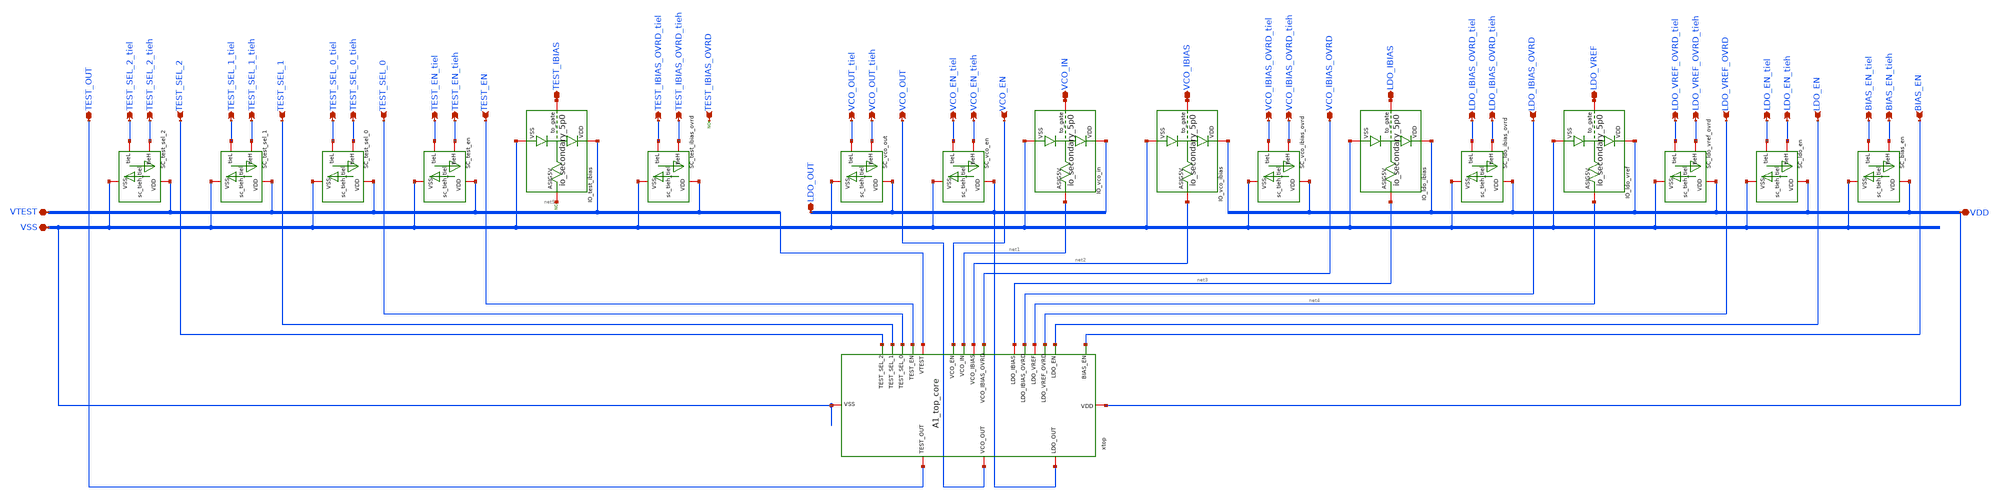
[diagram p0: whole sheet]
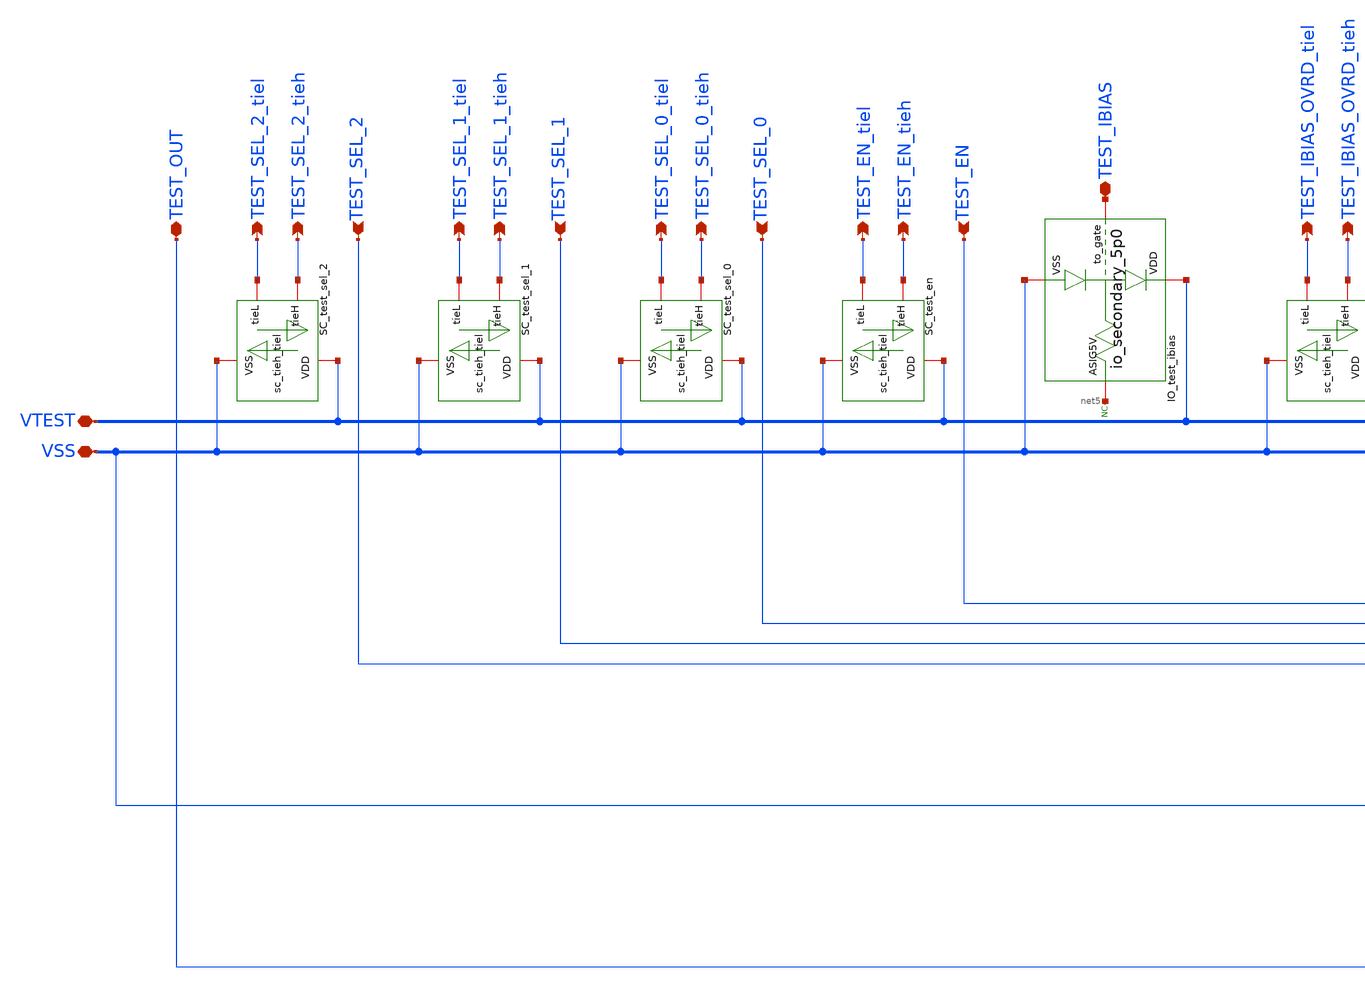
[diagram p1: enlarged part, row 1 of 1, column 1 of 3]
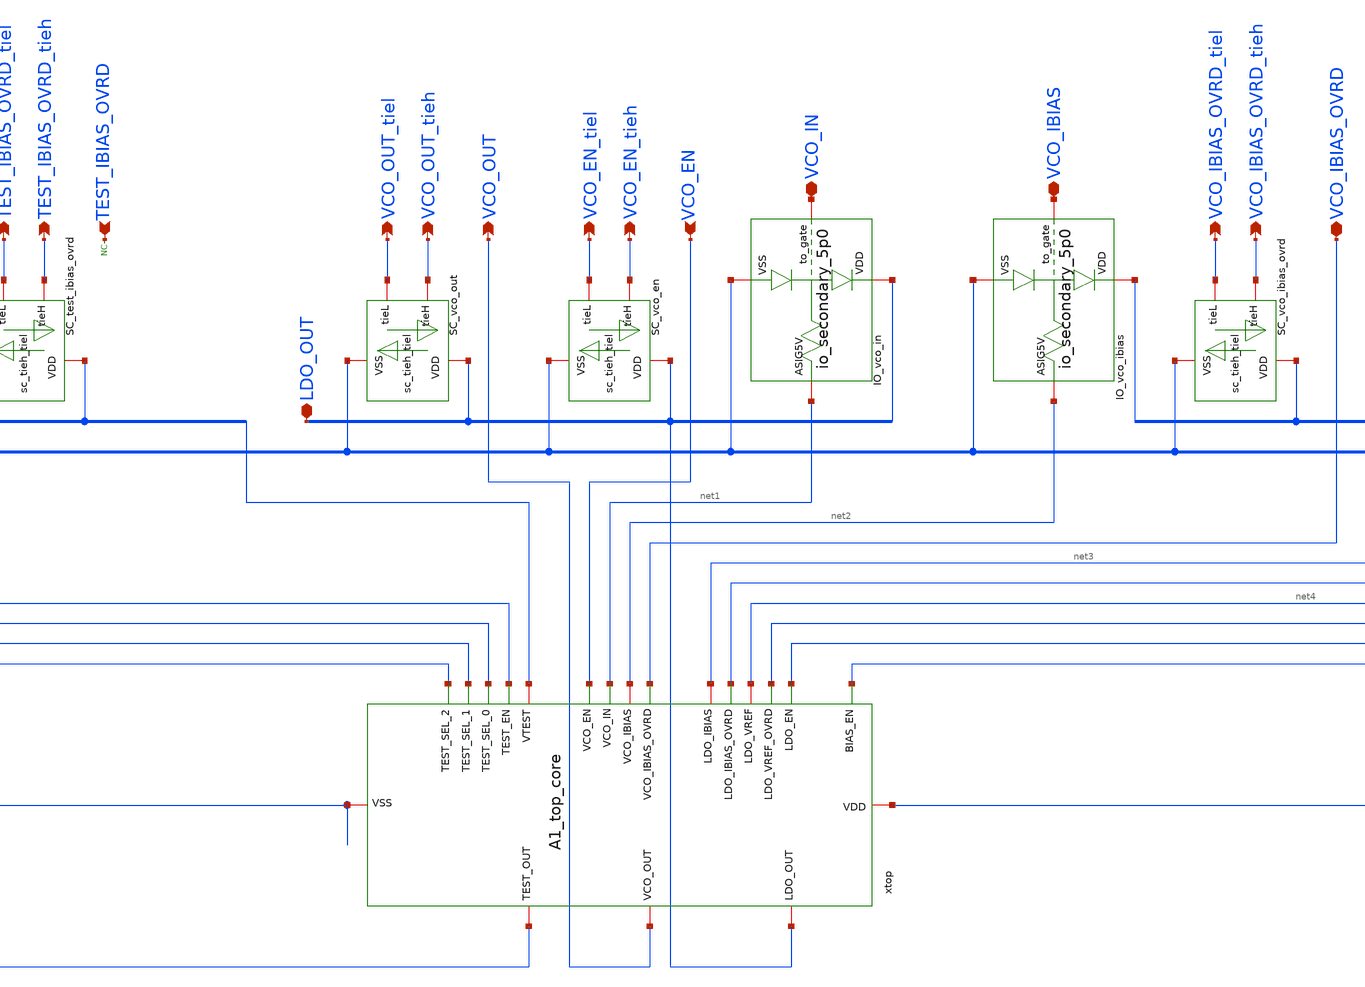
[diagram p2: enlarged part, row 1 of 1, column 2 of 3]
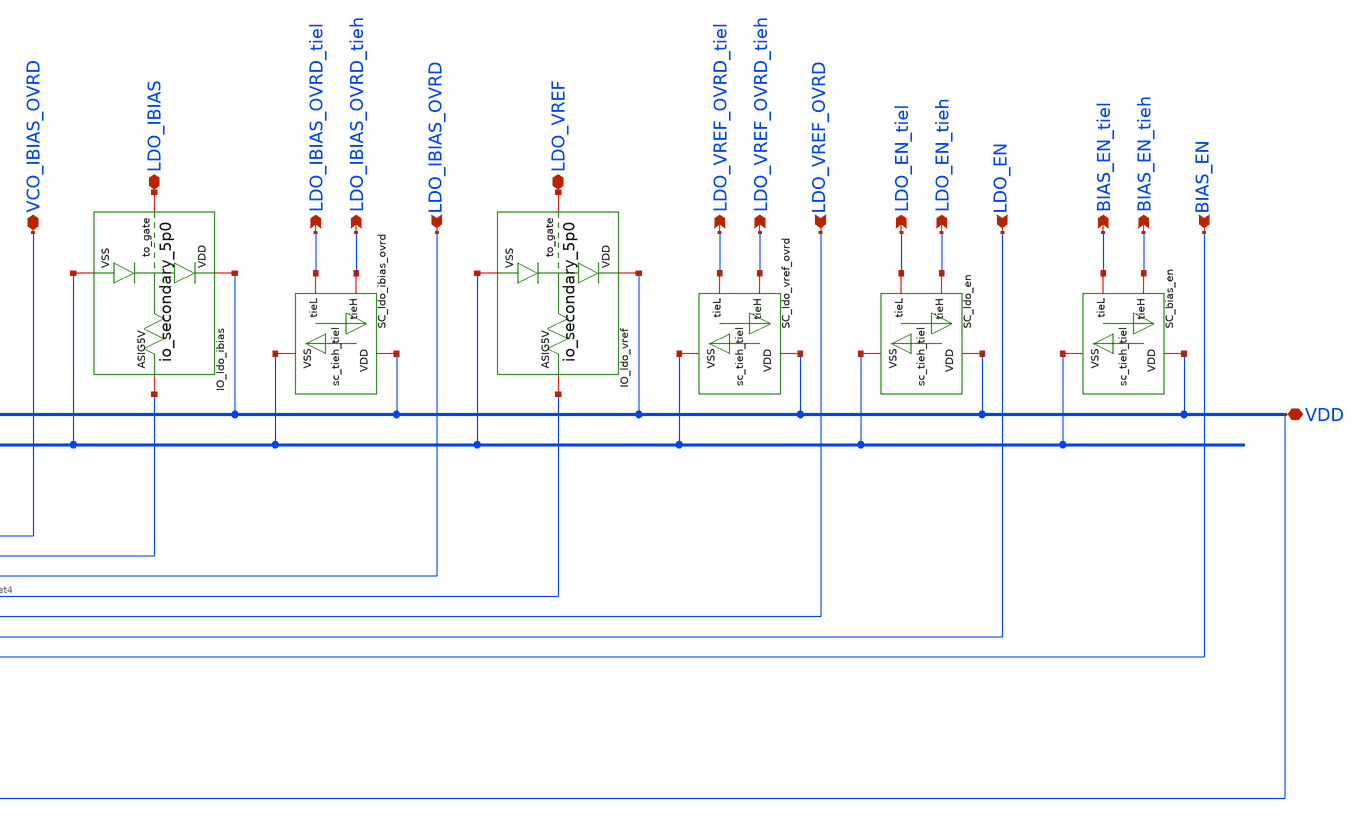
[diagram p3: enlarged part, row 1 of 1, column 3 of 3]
** sch_path: designs/libs/A1_core/A1_top/A1_top.sch
**.subckt A1_top TEST_SEL_2 TEST_SEL_2_tiel TEST_SEL_2_tieh VTEST VSS TEST_SEL_1 TEST_SEL_1_tiel
*+ TEST_SEL_1_tieh TEST_SEL_0 TEST_SEL_0_tiel TEST_SEL_0_tieh TEST_EN TEST_EN_tiel TEST_EN_tieh VCO_EN VCO_EN_tiel
*+ VCO_EN_tieh LDO_OUT VCO_OUT VCO_OUT_tiel VCO_OUT_tieh VCO_IBIAS_OVRD_tiel VCO_IBIAS_OVRD_tieh
*+ LDO_VREF_OVRD_tiel LDO_VREF_OVRD_tieh LDO_IBIAS_OVRD_tiel LDO_IBIAS_OVRD_tieh TEST_OUT VCO_IBIAS VCO_IBIAS_OVRD
*+ LDO_VREF LDO_VREF_OVRD LDO_IBIAS LDO_IBIAS_OVRD LDO_EN_tiel LDO_EN_tieh LDO_EN BIAS_EN_tiel BIAS_EN_tieh
*+ BIAS_EN VDD TEST_IBIAS_OVRD_tiel TEST_IBIAS_OVRD_tieh TEST_IBIAS TEST_IBIAS_OVRD VCO_IN
*.ipin TEST_SEL_2
*.opin TEST_SEL_2_tiel
*.opin TEST_SEL_2_tieh
*.iopin VTEST
*.iopin VSS
*.ipin TEST_SEL_1
*.opin TEST_SEL_1_tiel
*.opin TEST_SEL_1_tieh
*.ipin TEST_SEL_0
*.opin TEST_SEL_0_tiel
*.opin TEST_SEL_0_tieh
*.ipin TEST_EN
*.opin TEST_EN_tiel
*.opin TEST_EN_tieh
*.ipin VCO_EN
*.opin VCO_EN_tiel
*.opin VCO_EN_tieh
*.iopin LDO_OUT
*.opin VCO_OUT
*.opin VCO_OUT_tiel
*.opin VCO_OUT_tieh
*.opin VCO_IBIAS_OVRD_tiel
*.opin VCO_IBIAS_OVRD_tieh
*.opin LDO_VREF_OVRD_tiel
*.opin LDO_VREF_OVRD_tieh
*.opin LDO_IBIAS_OVRD_tiel
*.opin LDO_IBIAS_OVRD_tieh
*.iopin TEST_OUT
*.iopin VCO_IBIAS
*.iopin VCO_IBIAS_OVRD
*.iopin LDO_VREF
*.ipin LDO_VREF_OVRD
*.iopin LDO_IBIAS
*.ipin LDO_IBIAS_OVRD
*.opin LDO_EN_tiel
*.opin LDO_EN_tieh
*.ipin LDO_EN
*.opin BIAS_EN_tiel
*.opin BIAS_EN_tieh
*.ipin BIAS_EN
*.iopin VDD
*.opin TEST_IBIAS_OVRD_tiel
*.opin TEST_IBIAS_OVRD_tieh
*.iopin TEST_IBIAS
*.ipin TEST_IBIAS_OVRD
*.iopin VCO_IN
xtop VDD net1 LDO_OUT VCO_OUT VCO_EN TEST_OUT TEST_EN TEST_SEL_0 VSS VCO_IBIAS_OVRD net2 LDO_EN
+ LDO_IBIAS_OVRD net3 LDO_VREF_OVRD net4 TEST_SEL_1 TEST_SEL_2 VTEST BIAS_EN A1_top_core
XSC_test_sel_2 TEST_SEL_2_tiel VTEST VSS TEST_SEL_2_tieh sc_tieh_tiel
XSC_test_sel_1 TEST_SEL_1_tiel VTEST VSS TEST_SEL_1_tieh sc_tieh_tiel
XSC_test_sel_0 TEST_SEL_0_tiel VTEST VSS TEST_SEL_0_tieh sc_tieh_tiel
XSC_test_en TEST_EN_tiel VTEST VSS TEST_EN_tieh sc_tieh_tiel
XSC_vco_en VCO_EN_tiel LDO_OUT VSS VCO_EN_tieh sc_tieh_tiel
XSC_vco_out VCO_OUT_tiel LDO_OUT VSS VCO_OUT_tieh sc_tieh_tiel
XSC_vco_ibias_ovrd VCO_IBIAS_OVRD_tiel VDD VSS VCO_IBIAS_OVRD_tieh sc_tieh_tiel
XSC_ldo_ibias_ovrd LDO_IBIAS_OVRD_tiel VDD VSS LDO_IBIAS_OVRD_tieh sc_tieh_tiel
XSC_ldo_vref_ovrd LDO_VREF_OVRD_tiel VDD VSS LDO_VREF_OVRD_tieh sc_tieh_tiel
XSC_ldo_en LDO_EN_tiel VDD VSS LDO_EN_tieh sc_tieh_tiel
XSC_bias_en BIAS_EN_tiel VDD VSS BIAS_EN_tieh sc_tieh_tiel
XSC_test_ibias_ovrd TEST_IBIAS_OVRD_tiel VTEST VSS TEST_IBIAS_OVRD_tieh sc_tieh_tiel
* noconn #net5
* noconn TEST_IBIAS_OVRD
XIO_test_ibias VTEST TEST_IBIAS net5 VSS io_secondary_5p0
XIO_vco_in LDO_OUT VCO_IN net1 VSS io_secondary_5p0
XIO_vco_ibias VDD VCO_IBIAS net2 VSS io_secondary_5p0
XIO_ldo_ibias VDD LDO_IBIAS net3 VSS io_secondary_5p0
XIO_ldo_vref VDD LDO_VREF net4 VSS io_secondary_5p0
**.ends
.end
